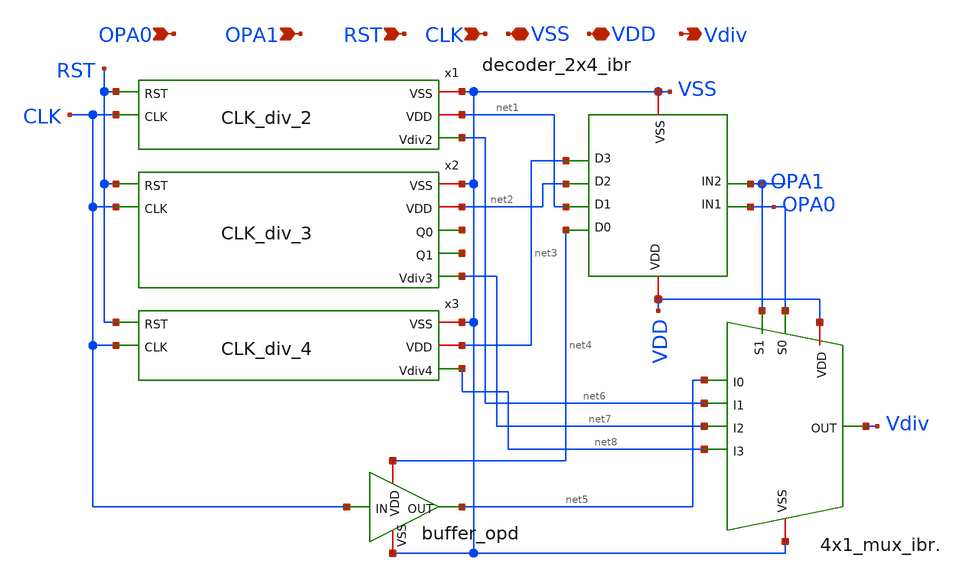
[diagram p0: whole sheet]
** sch_path: Clock_Generator_PAKISTAN_02/Schematics/Prescaler_Divider.sch
**.subckt Prescaler_Divider CLK VSS VDD RST Vdiv OPA1 OPA0
*.ipin CLK
*.iopin VSS
*.iopin VDD
*.ipin RST
*.opin Vdiv
*.ipin OPA1
*.ipin OPA0
x1 VSS net1 net6 RST CLK CLK_div_2
x2 VSS net2 net9 net10 RST net7 CLK CLK_div_3
x3 VSS net3 net8 RST CLK CLK_div_4
x4 VDD OPA1 VSS net7 net8 OPA0 net5 net6 Vdiv 4x1_mux_ibr.
x5 OPA0 VSS VDD net4 net1 net2 net3 OPA1 decoder_2x4_ibr
x6 VSS CLK net5 net4 buffer_opd
**.ends
.end
